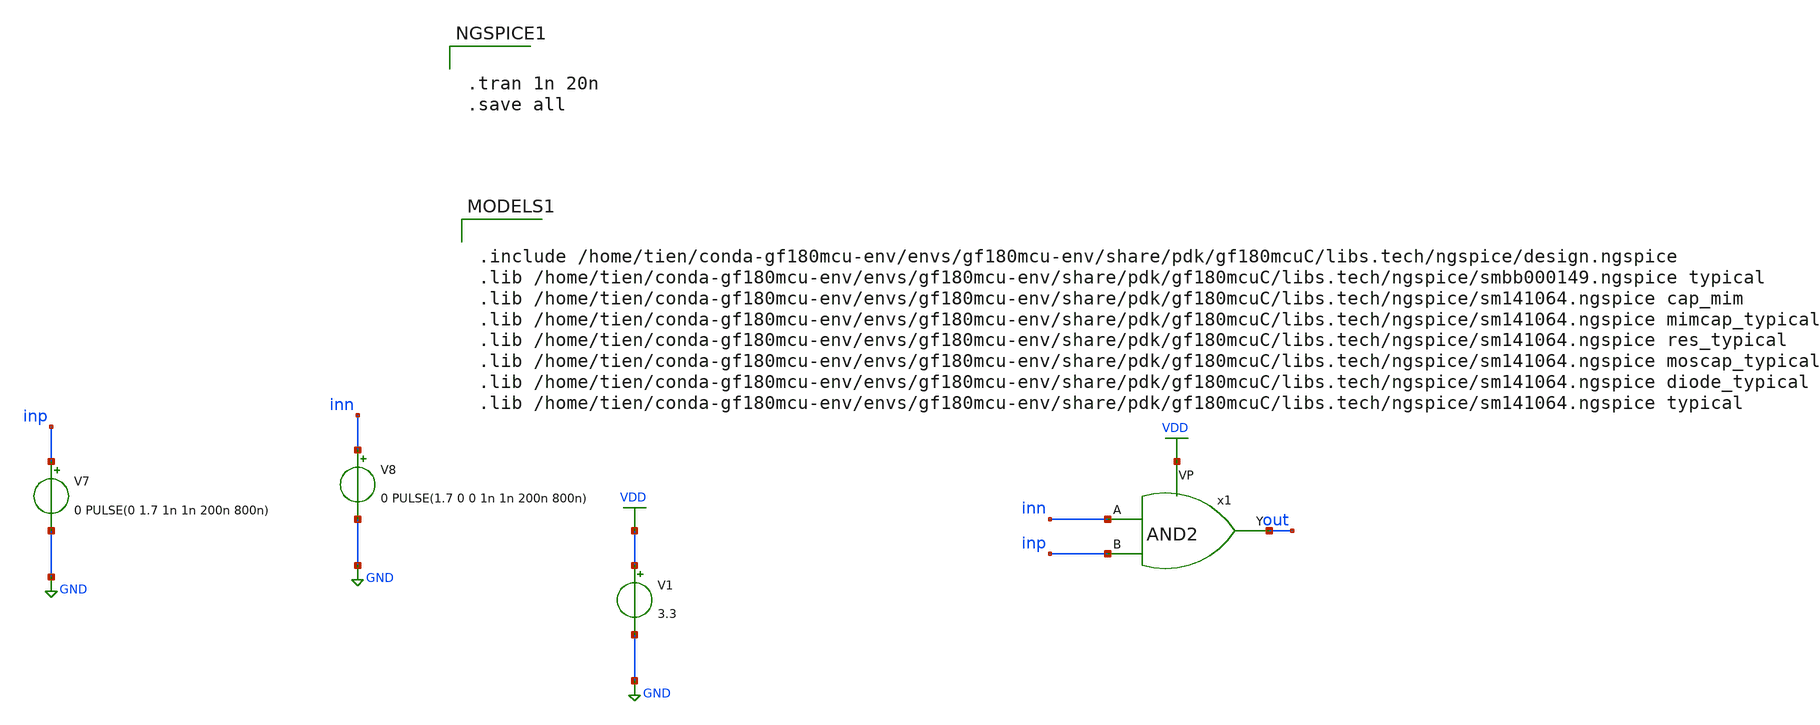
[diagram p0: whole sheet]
** sch_path: tesst2.sch
**.subckt tesst2
V7 inp GND 0 PULSE(0 1.7 1n 1n 200n 800n)
V8 inn GND 0 PULSE(1.7 0 0 1n 1n 200n 800n)
x1 VDD inn inp out AND2
V1 VDD GND 3.3
**** begin user architecture code


.tran 1n 20n
.save all



.include /home/tien/conda-gf180mcu-env/envs/gf180mcu-env/share/pdk/gf180mcuC/libs.tech/ngspice/design.ngspice
.lib /home/tien/conda-gf180mcu-env/envs/gf180mcu-env/share/pdk/gf180mcuC/libs.tech/ngspice/smbb000149.ngspice typical
.lib /home/tien/conda-gf180mcu-env/envs/gf180mcu-env/share/pdk/gf180mcuC/libs.tech/ngspice/sm141064.ngspice cap_mim
.lib /home/tien/conda-gf180mcu-env/envs/gf180mcu-env/share/pdk/gf180mcuC/libs.tech/ngspice/sm141064.ngspice mimcap_typical
.lib /home/tien/conda-gf180mcu-env/envs/gf180mcu-env/share/pdk/gf180mcuC/libs.tech/ngspice/sm141064.ngspice res_typical
.lib /home/tien/conda-gf180mcu-env/envs/gf180mcu-env/share/pdk/gf180mcuC/libs.tech/ngspice/sm141064.ngspice moscap_typical
.lib /home/tien/conda-gf180mcu-env/envs/gf180mcu-env/share/pdk/gf180mcuC/libs.tech/ngspice/sm141064.ngspice diode_typical
.lib /home/tien/conda-gf180mcu-env/envs/gf180mcu-env/share/pdk/gf180mcuC/libs.tech/ngspice/sm141064.ngspice typical

**** end user architecture code
**.ends

* expanding   symbol:  AND2.sym # of pins=4
** sym_path: AND2.sym
** sch_path: AND2.sch
.subckt AND2 VP A B Y
*.ipin A
*.ipin B
*.opin Y
*.iopin VP
XM1 net1 B net2 GND nfet_03v3 L=0.28u W=0.22u nf=1 ad='int((nf+1)/2) * W/nf * 0.18u' as='int((nf+2)/2) * W/nf * 0.18u'
+ pd='2*int((nf+1)/2) * (W/nf + 0.18u)' ps='2*int((nf+2)/2) * (W/nf + 0.18u)' nrd='0.18u / W' nrs='0.18u / W'
+ sa=0 sb=0 sd=0 m=1
XM2 net1 A VP VP pfet_03v3 L=0.28u W=1u nf=1 ad='int((nf+1)/2) * W/nf * 0.18u' as='int((nf+2)/2) * W/nf * 0.18u'
+ pd='2*int((nf+1)/2) * (W/nf + 0.18u)' ps='2*int((nf+2)/2) * (W/nf + 0.18u)' nrd='0.18u / W' nrs='0.18u / W'
+ sa=0 sb=0 sd=0 m=1
XM4 net2 A GND GND nfet_03v3 L=0.28u W=0.22u nf=1 ad='int((nf+1)/2) * W/nf * 0.18u' as='int((nf+2)/2) * W/nf * 0.18u'
+ pd='2*int((nf+1)/2) * (W/nf + 0.18u)' ps='2*int((nf+2)/2) * (W/nf + 0.18u)' nrd='0.18u / W' nrs='0.18u / W'
+ sa=0 sb=0 sd=0 m=1
XM5 Y net1 VP VP pfet_03v3 L=0.28u W=1u nf=1 ad='int((nf+1)/2) * W/nf * 0.18u' as='int((nf+2)/2) * W/nf * 0.18u'
+ pd='2*int((nf+1)/2) * (W/nf + 0.18u)' ps='2*int((nf+2)/2) * (W/nf + 0.18u)' nrd='0.18u / W' nrs='0.18u / W'
+ sa=0 sb=0 sd=0 m=1
XM6 Y net1 GND GND nfet_03v3 L=0.28u W=0.22u nf=1 ad='int((nf+1)/2) * W/nf * 0.18u' as='int((nf+2)/2) * W/nf * 0.18u'
+ pd='2*int((nf+1)/2) * (W/nf + 0.18u)' ps='2*int((nf+2)/2) * (W/nf + 0.18u)' nrd='0.18u / W' nrs='0.18u / W'
+ sa=0 sb=0 sd=0 m=1
XM3 net1 B VP VP pfet_03v3 L=0.28u W=1u nf=1 ad='int((nf+1)/2) * W/nf * 0.18u' as='int((nf+2)/2) * W/nf * 0.18u'
+ pd='2*int((nf+1)/2) * (W/nf + 0.18u)' ps='2*int((nf+2)/2) * (W/nf + 0.18u)' nrd='0.18u / W' nrs='0.18u / W'
+ sa=0 sb=0 sd=0 m=1
.ends

.GLOBAL GND
.GLOBAL VDD
.end
